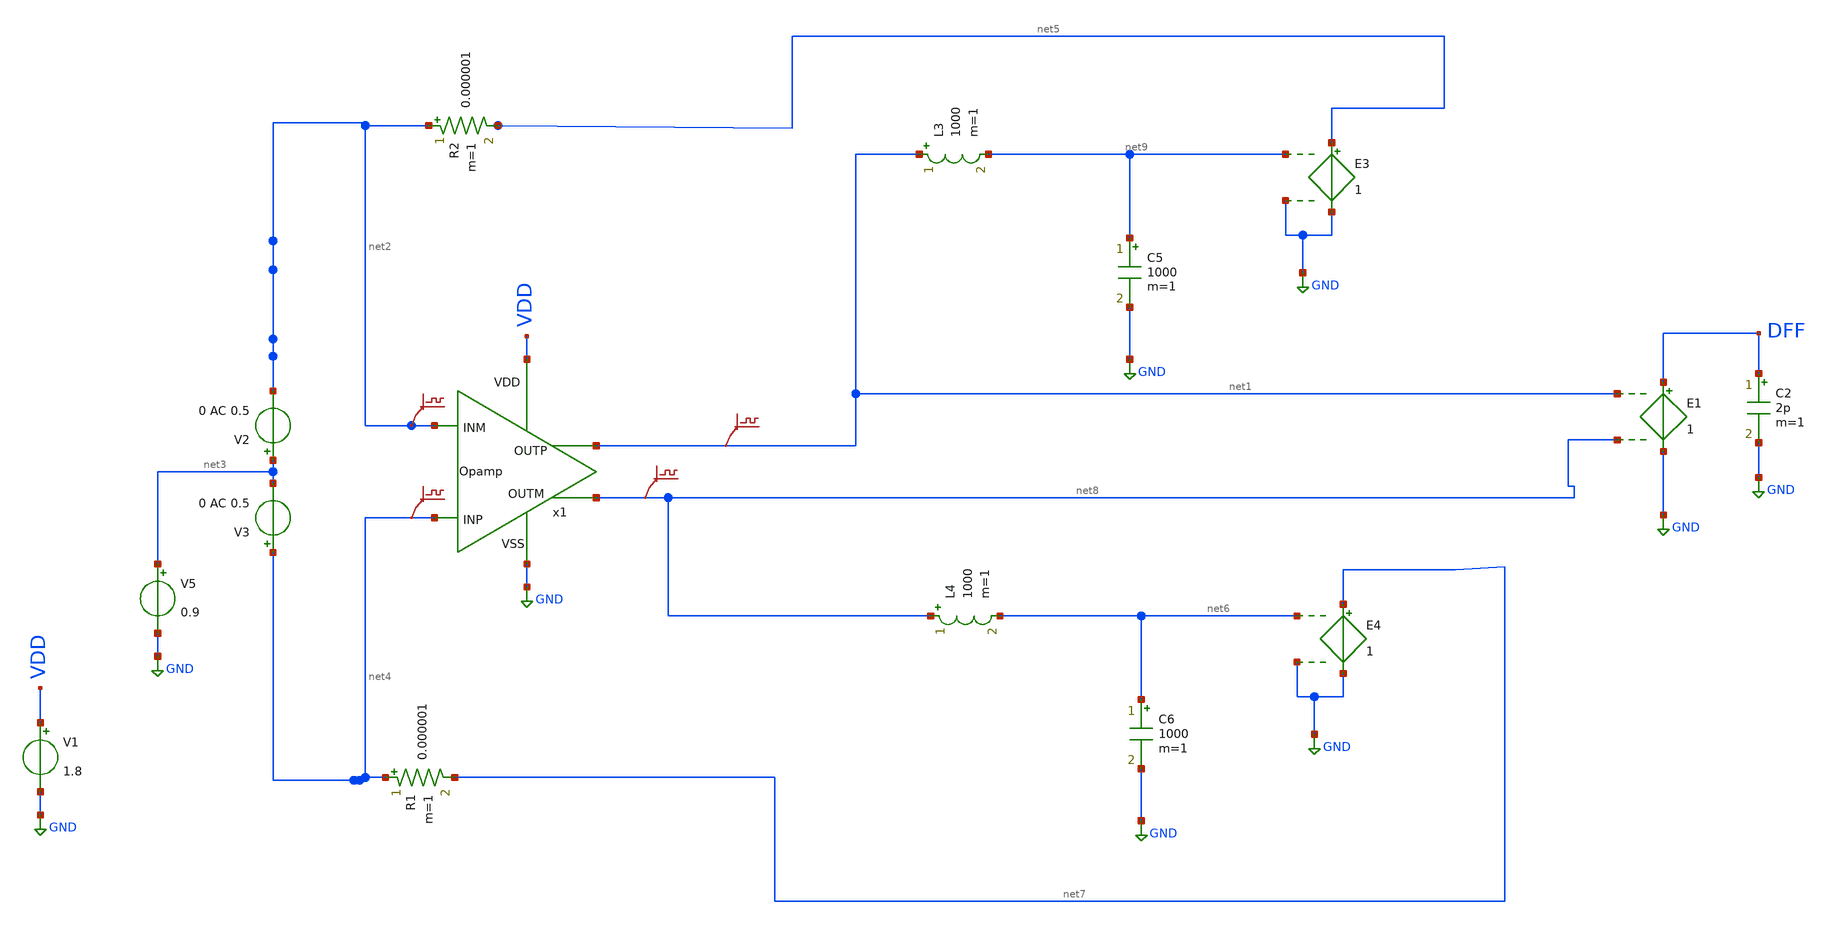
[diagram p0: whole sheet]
** sch_path: Opamp_IdealSupply.sch
**.subckt Opamp_IdealSupply
.save v(net1)
.save v(net8)
.save v(net2)
.save v(net4)
V2 net3 net2 0 AC 0.5
V5 net3 GND 0.9
V3 net4 net3 0 AC 0.5
V1 VDD GND 1.8
R2 net2 net5 0.000001 m=1
R1 net4 net7 0.000001 m=1
L3 net1 net9 1000 m=1
C5 net9 GND 1000 m=1
E3 net5 GND net9 GND 1
L4 net8 net6 1000 m=1
C6 net6 GND 1000 m=1
E4 net7 GND net6 GND 1
E1 DFF GND net1 net8 1
C2 DFF GND 2p m=1
x1 net1 net2 net4 GND VDD net8 Opamp
**** begin user architecture code



.control

save all

op
write untitled-10.raw

ac dec 10 1 10e9
set appendwrite
write untitled-10.raw

*plot db((v(out)-v(outn))/(v(net3)-v(net1))) 180*cph(v(out)-v(outn))/pi
plot db(v(dff)/(V(net4)-V(net2))) 180*cph(v(dff))/pi
*plot db(v(outn)) 180*cph(v(outn))/pi
.endc



** opencircuitdesign pdks install
.lib $::SKYWATER_MODELS/sky130.lib.spice tt


**** end user architecture code
**.ends
.GLOBAL GND
.end
